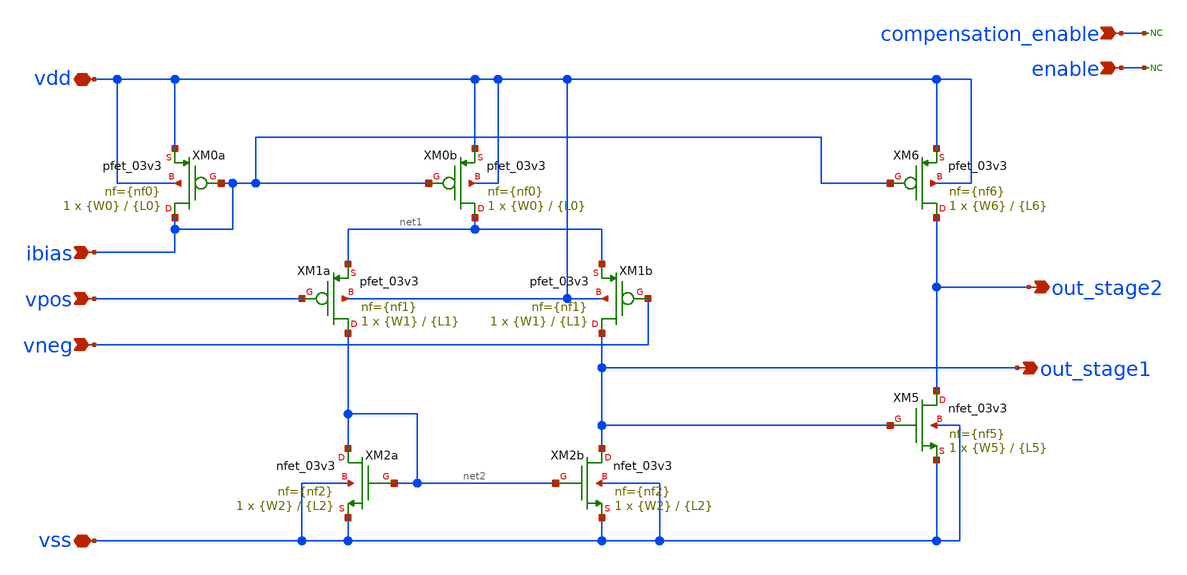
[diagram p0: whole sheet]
** sch_path: DESIGN/DACFUTURE_EDU/Two_stage_OTA/two_stage_ota.sch
**.subckt two_stage_ota enable vpos vneg vdd vss compensation_enable out_stage2 ibias
*.ipin enable
*.ipin vpos
*.ipin vneg
*.iopin vdd
*.iopin vss
*.ipin compensation_enable
*.opin out_stage2
*.ipin ibias
XM0a ibias ibias vdd vdd pfet_03v3 L={L0} W={W0} nf={nf0} ad='int((nf0+1)/2) * W0/nf0 * 0.18u' as='int((nf0+2)/2) * W0/nf0 * 0.18u'
+ pd='2*int((nf0+1)/2) * (W0/nf0 + 0.18u)' ps='2*int((nf0+2)/2) * (W0/nf0 + 0.18u)' nrd='0.18u / W0' nrs='0.18u / W0'
+ sa=0 sb=0 sd=0 m=1
XM0b net1 ibias vdd vdd pfet_03v3 L={L0} W={W0} nf={nf0} ad='int((nf0+1)/2) * W0/nf0 * 0.18u' as='int((nf0+2)/2) * W0/nf0 * 0.18u'
+ pd='2*int((nf0+1)/2) * (W0/nf0 + 0.18u)' ps='2*int((nf0+2)/2) * (W0/nf0 + 0.18u)' nrd='0.18u / W0' nrs='0.18u / W0'
+ sa=0 sb=0 sd=0 m=1
XM1a net2 vpos net1 vdd pfet_03v3 L={L1} W={W1} nf={nf1} ad='int((nf1+1)/2) * W1/nf1 * 0.18u' as='int((nf1+2)/2) * W1/nf1 * 0.18u'
+ pd='2*int((nf1+1)/2) * (W1/nf1 + 0.18u)' ps='2*int((nf1+2)/2) * (W1/nf1 + 0.18u)' nrd='0.18u / W1' nrs='0.18u / W1'
+ sa=0 sb=0 sd=0 m=1
XM1b out_stage1 vneg net1 vdd pfet_03v3 L={L1} W={W1} nf={nf1} ad='int((nf1+1)/2) * W1/nf1 * 0.18u' as='int((nf1+2)/2) * W1/nf1 * 0.18u'
+ pd='2*int((nf1+1)/2) * (W1/nf1 + 0.18u)' ps='2*int((nf1+2)/2) * (W1/nf1 + 0.18u)' nrd='0.18u / W1' nrs='0.18u / W1'
+ sa=0 sb=0 sd=0 m=1
XM2b out_stage1 net2 vss vss nfet_03v3 L={L2} W={W2} nf={nf2} ad='int((nf2+1)/2) * W2/nf2 * 0.18u' as='int((nf2+2)/2) * W2/nf2 * 0.18u'
+ pd='2*int((nf2+1)/2) * (W2/nf2 + 0.18u)' ps='2*int((nf2+2)/2) * (W2/nf2 + 0.18u)' nrd='0.18u / W2' nrs='0.18u / W2'
+ sa=0 sb=0 sd=0 m=1
XM2a net2 net2 vss vss nfet_03v3 L={L2} W={W2} nf={nf2} ad='int((nf2+1)/2) * W2/nf2 * 0.18u' as='int((nf2+2)/2) * W2/nf2 * 0.18u'
+ pd='2*int((nf2+1)/2) * (W2/nf2 + 0.18u)' ps='2*int((nf2+2)/2) * (W2/nf2 + 0.18u)' nrd='0.18u / W2' nrs='0.18u / W2'
+ sa=0 sb=0 sd=0 m=1
XM6 out_stage2 ibias vdd vdd pfet_03v3 L={L6} W={W6} nf={nf6} ad='int((nf6+1)/2) * W6/nf6 * 0.18u' as='int((nf6+2)/2) * W6/nf6 * 0.18u'
+ pd='2*int((nf6+1)/2) * (W6/nf6 + 0.18u)' ps='2*int((nf6+2)/2) * (W6/nf6 + 0.18u)' nrd='0.18u / W6' nrs='0.18u / W6'
+ sa=0 sb=0 sd=0 m=1
XM5 out_stage2 out_stage1 vss vss nfet_03v3 L={L5} W={W5} nf={nf5} ad='int((nf5+1)/2) * W5/nf5 * 0.18u'
+ as='int((nf5+2)/2) * W5/nf5 * 0.18u' pd='2*int((nf5+1)/2) * (W5/nf5 + 0.18u)' ps='2*int((nf5+2)/2) * (W5/nf5 + 0.18u)'
+ nrd='0.18u / W5' nrs='0.18u / W5' sa=0 sb=0 sd=0 m=1
* noconn compensation_enable
* noconn enable
**.ends
.end
